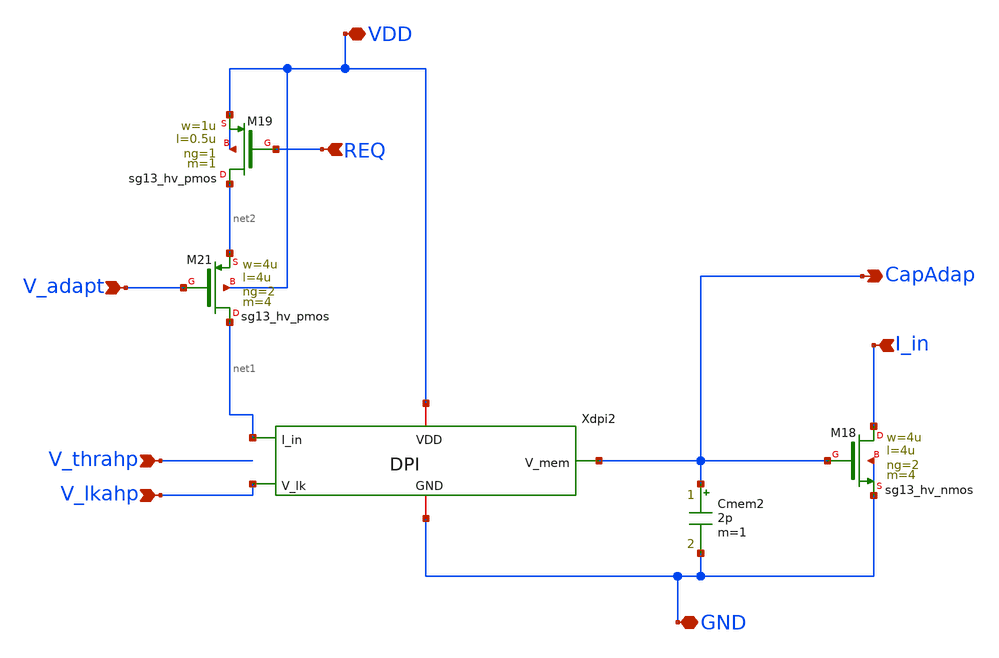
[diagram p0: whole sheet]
** sch_path: xschem/ADAP_system.sch
**.subckt ADAP_system VDD GND REQ V_adapt V_thrahp V_lkahp I_in CapAdap
*.iopin VDD
*.iopin GND
*.ipin REQ
*.ipin V_adapt
*.ipin V_thrahp
*.ipin V_lkahp
*.ipin I_in
*.opin CapAdap
XM19 net2 REQ VDD VDD sg13_hv_pmos w=1u l=0.5u ng=1 m=1 mm_ok=1
XM21 net1 V_adapt net2 VDD sg13_hv_pmos w=4u l=4u ng=2 m=4 mm_ok=1
XM18 I_in CapAdap GND GND sg13_hv_nmos w=4u l=4u ng=2 m=4 mm_ok=1
Cmem2 CapAdap GND 2p m=1
Xdpi2 net1 VDD CapAdap V_lkahp GND DPI
**.ends
.end
